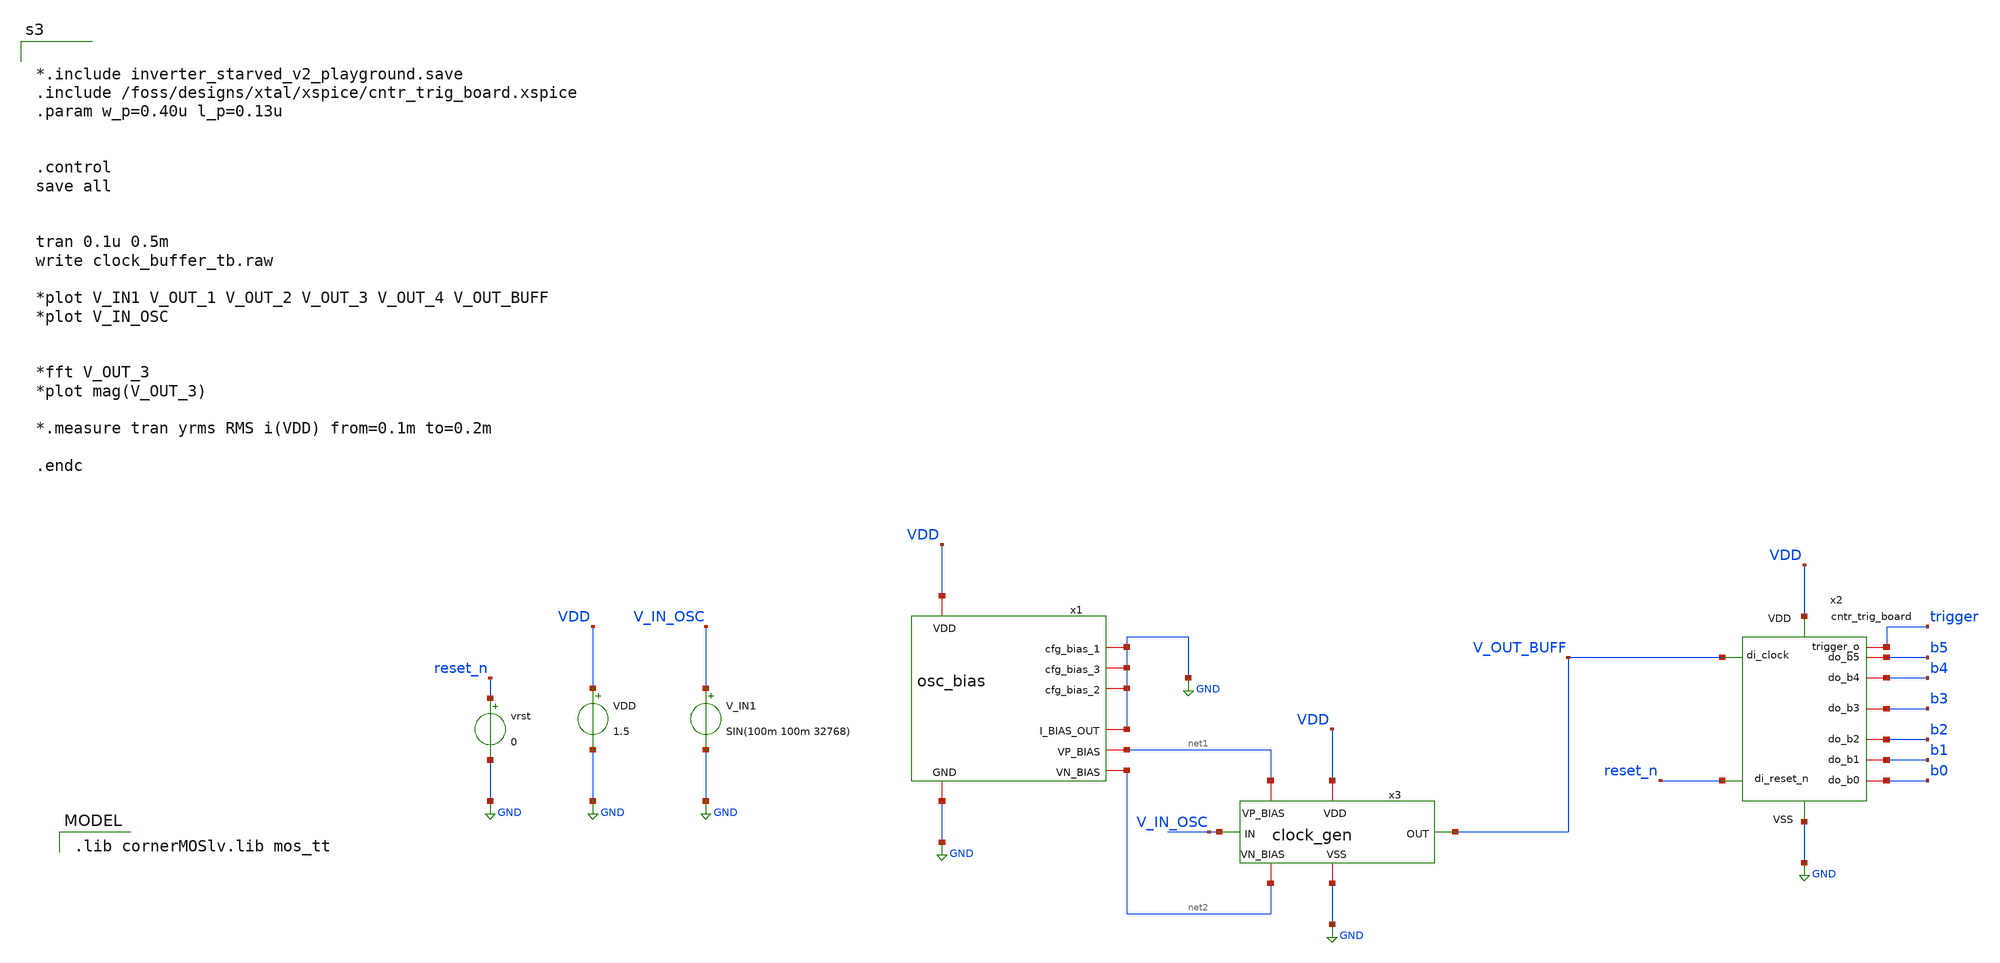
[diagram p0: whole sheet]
** sch_path: clock_buffer_tb.sch
**.subckt clock_buffer_tb
x1 VDD GND GND GND GND GND net1 net2 osc_bias
x2 VDD GND V_OUT_BUFF b0 b1 b2 b3 b4 b5 reset_n trigger cntr_trig_board
vrst reset_n GND 0
VDD VDD GND 1.5
x3 VDD V_IN_OSC V_OUT_BUFF GND net1 net2 clock_gen
V_IN1 V_IN_OSC GND SIN(100m 100m 32768)
**** begin user architecture code


*.include inverter_starved_v2_playground.save
.include /foss/designs/xtal/xspice/cntr_trig_board.xspice
.param w_p=0.40u l_p=0.13u


.control
save all


tran 0.1u 0.5m
write clock_buffer_tb.raw

*plot V_IN1 V_OUT_1 V_OUT_2 V_OUT_3 V_OUT_4 V_OUT_BUFF
*plot V_IN_OSC


*fft V_OUT_3
*plot mag(V_OUT_3)

*.measure tran yrms RMS i(VDD) from=0.1m to=0.2m

.endc


 .lib cornerMOSlv.lib mos_tt

**** end user architecture code
**.ends

* expanding   symbol:  osc_bias.sym # of pins=8
** sym_path: osc_bias.sym
** sch_path: osc_bias.sch
.subckt osc_bias VDD cfg_bias_1 cfg_bias_3 cfg_bias_2 GND I_BIAS_OUT VP_BIAS VN_BIAS
*.iopin VDD
*.iopin GND
*.iopin I_BIAS_OUT
*.iopin cfg_bias_1
*.iopin cfg_bias_2
*.iopin cfg_bias_3
*.opin VN_BIAS
*.opin VP_BIAS
XM1 net1 net1 VDD VDD sg13_lv_pmos w=0.25u l=10u ng=1 m=1 mm_ok=1
XM3 net1 net1 net2 GND sg13_lv_nmos w=0.25u l=10u ng=1 m=1 mm_ok=1
XM4 net2 net2 net3 GND sg13_lv_nmos w=0.25u l=10u ng=1 m=1 mm_ok=1
XM5 net3 net3 net14 GND sg13_lv_nmos w=0.25u l=10u ng=1 m=1 mm_ok=1
XM2 net9 net1 VDD VDD sg13_lv_pmos w=0.25u l=10u ng=1 m=2 mm_ok=1
XM6 net4 cfg_bias_1 net9 VDD sg13_lv_pmos w=0.25u l=10u ng=1 m=1 mm_ok=1
XM7 net5 net1 VDD VDD sg13_lv_pmos w=0.25u l=10u ng=1 m=4 mm_ok=1
XM8 net6 net1 VDD VDD sg13_lv_pmos w=0.25u l=10u ng=1 m=20 mm_ok=1
XM9 net4 cfg_bias_2 net5 VDD sg13_lv_pmos w=0.5u l=10u ng=1 m=1 mm_ok=1
XM10 net4 cfg_bias_3 net6 VDD sg13_lv_pmos w=1u l=10u ng=1 m=1 mm_ok=1
XM11 net7 net7 net8 GND sg13_lv_nmos w=0.2u l=10u ng=1 m=1 mm_ok=1
Vmeas net8 GND 0
.save i(vmeas)
XM12 VP_BIAS VP_BIAS net12 VDD sg13_lv_pmos w=0.8u l=0.13u ng=1 m=1 mm_ok=1
XM13 VN_BIAS VN_BIAS net11 GND sg13_lv_nmos w=0.4u l=0.13u ng=1 m=1 mm_ok=1
Vmeas1 VDD net12 0
.save i(vmeas1)
Vmeas2 net11 GND 0
.save i(vmeas2)
XM14 net10 net10 VN_BIAS GND sg13_lv_nmos w=0.4u l=10u ng=1 m=1 mm_ok=1
XM15 net13 net13 net10 GND sg13_lv_nmos w=0.4u l=10u ng=1 m=1 mm_ok=1
XM16 VP_BIAS VP_BIAS net13 GND sg13_lv_nmos w=0.4u l=10u ng=1 m=1 mm_ok=1
XM17 net14 net14 net7 GND sg13_lv_nmos w=0.25u l=10u ng=1 m=1 mm_ok=1
Vmeas3 net4 I_BIAS_OUT 0
.save i(vmeas3)
.ends


* expanding   symbol:  clock_gen.sym # of pins=6
** sym_path: clock_gen.sym
** sch_path: clock_gen.sch
.subckt clock_gen VDD IN OUT VSS VP_BIAS VN_BIAS
*.ipin IN
*.iopin VSS
*.opin OUT
*.iopin VDD
*.ipin VP_BIAS
*.ipin VN_BIAS
XM13 V_OUT_1 V_IN_1 net2 VSS sg13_lv_nmos w={w_p} l={l_p} ng=1 m=1 mm_ok=1
XM14 V_OUT_1 V_IN_1 M2_Source VDD sg13_lv_pmos w={2*{w_p}} l={l_p} ng=1 m=1 mm_ok=1
XM15 net3 VN_BIAS VSS VSS sg13_lv_nmos w={w_p} l={l_p} ng=1 m=1 mm_ok=1
XM16 net1 VP_BIAS VDD VDD sg13_lv_pmos w={2*{w_p}} l={l_p} ng=1 m=1 mm_ok=1
Vmeas_PMOS1 net1 M2_Source 0
.save i(vmeas_pmos1)
Vmeas_NMOS1 net2 net3 0
.save i(vmeas_nmos1)
C2 IN V_IN_1 50p m=1
XM17 V_OUT_2 V_OUT_1 net4 VSS sg13_lv_nmos w={w_p} l={l_p} ng=1 m=1 mm_ok=1
XM18 V_OUT_2 V_OUT_1 net6 VDD sg13_lv_pmos w={2*{w_p}} l={l_p} ng=1 m=1 mm_ok=1
Vmeas_NMOS2 net4 net7 0
.save i(vmeas_nmos2)
XM19 net5 VP_BIAS VDD VDD sg13_lv_pmos w={2*{w_p}} l={l_p} ng=1 m=1 mm_ok=1
Vmeas_PMOS2 net5 net6 0
.save i(vmeas_pmos2)
XM20 net7 VN_BIAS VSS VSS sg13_lv_nmos w={w_p} l={l_p} ng=1 m=1 mm_ok=1
XM21 OUT V_OUT_4 net10 VSS sg13_lv_nmos w={w_p} l={l_p} ng=1 m=1 mm_ok=1
XM22 OUT V_OUT_4 net9 VDD sg13_lv_pmos w={2*{w_p}} l={l_p} ng=1 m=1 mm_ok=1
XM23 V_OUT_1 net8 net8 net8 sg13_lv_pmos w=0.5u l=2u ng=1 m=1 mm_ok=1
XM24 net8 V_IN_1 V_IN_1 V_IN_1 sg13_lv_pmos w=0.5u l=2u ng=1 m=1 mm_ok=1
Vmeas_PMOS_OUT VDD net9 0
.save i(vmeas_pmos_out)
Vmeas_NMOS_OUT net10 VSS 0
.save i(vmeas_nmos_out)
XM25 V_OUT_3 V_OUT_2 net11 VSS sg13_lv_nmos w={w_p} l={l_p} ng=1 m=1 mm_ok=1
XM26 V_OUT_3 V_OUT_2 net13 VDD sg13_lv_pmos w={2*{w_p}} l={l_p} ng=1 m=1 mm_ok=1
Vmeas_NMOS3 net11 net14 0
.save i(vmeas_nmos3)
XM27 net12 VP_BIAS VDD VDD sg13_lv_pmos w={2*{w_p}} l={l_p} ng=1 m=1 mm_ok=1
Vmeas_PMOS3 net12 net13 0
.save i(vmeas_pmos3)
XM28 net14 VN_BIAS VSS VSS sg13_lv_nmos w={w_p} l={l_p} ng=1 m=1 mm_ok=1
XM29 V_OUT_4 V_OUT_3 net15 VSS sg13_lv_nmos w={w_p} l={l_p} ng=1 m=1 mm_ok=1
XM30 V_OUT_4 V_OUT_3 net17 VDD sg13_lv_pmos w={2*{w_p}} l={l_p} ng=1 m=1 mm_ok=1
Vmeas_NMOS4 net15 net18 0
.save i(vmeas_nmos4)
XM31 net16 VP_BIAS VDD VDD sg13_lv_pmos w={2*{w_p}} l={l_p} ng=1 m=1 mm_ok=1
Vmeas_PMOS4 net16 net17 0
.save i(vmeas_pmos4)
XM32 net18 VN_BIAS VSS VSS sg13_lv_nmos w={w_p} l={l_p} ng=1 m=1 mm_ok=1
.ends

.GLOBAL GND
.end
